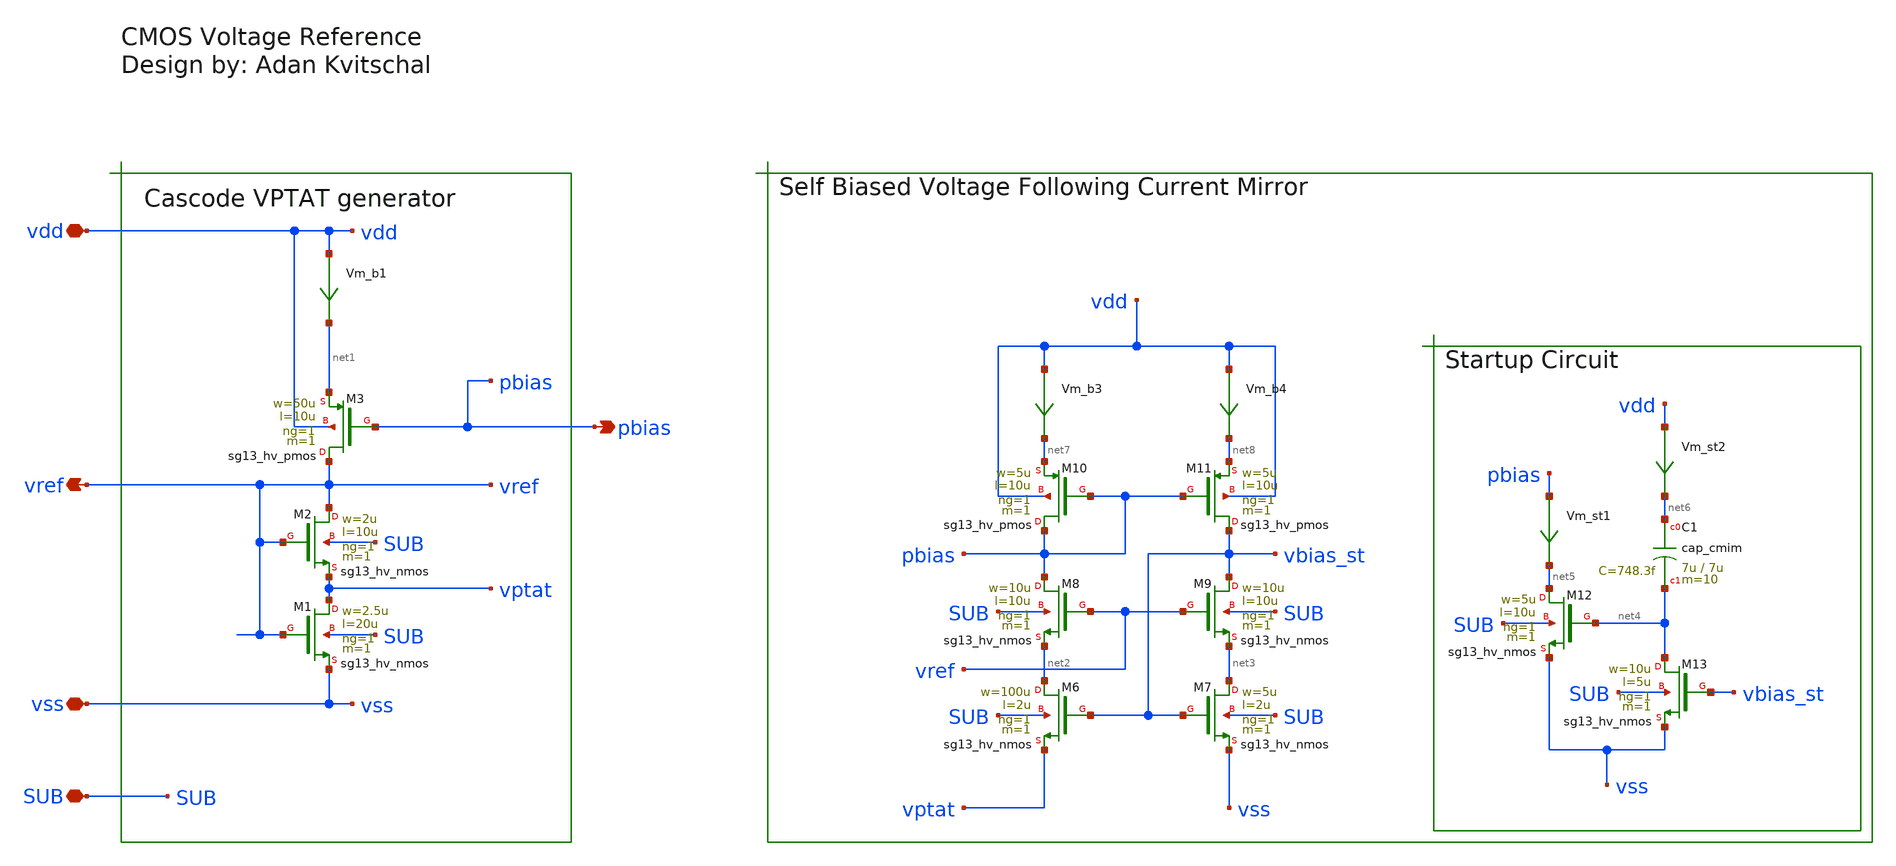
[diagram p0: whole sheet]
** sch_path: release/xschem/sch/cmos_vref.sch
**.subckt cmos_vref vss SUB vdd pbias vref
*.iopin vss
*.iopin SUB
*.iopin vdd
*.opin pbias
*.opin vref
Vm_b1 vdd net1 0
.save i(vm_b1)
XM1 vptat vref vss SUB sg13_hv_nmos w=2.5u l=20u ng=1 m=1 mm_ok=1
XM2 vref vref vptat SUB sg13_hv_nmos w=2u l=10u ng=1 m=1 mm_ok=1
XM3 vref pbias net1 vdd sg13_hv_pmos w=50u l=10u ng=1 m=1 mm_ok=1
Vm_st1 pbias net5 0
.save i(vm_st1)
Vm_st2 vdd net6 0
.save i(vm_st2)
Vm_b3 vdd net7 0
.save i(vm_b3)
Vm_b4 vdd net8 0
.save i(vm_b4)
XM7 net3 vbias_st vss SUB sg13_hv_nmos w=5u l=2u ng=1 m=1 mm_ok=1
XM11 vbias_st pbias net8 vdd sg13_hv_pmos w=5u l=10u ng=1 m=1 mm_ok=1
XM6 net2 vbias_st vptat SUB sg13_hv_nmos w=100u l=2u ng=1 m=1 mm_ok=1
XM9 vbias_st vref net3 SUB sg13_hv_nmos w=10u l=10u ng=1 m=1 mm_ok=1
XM8 pbias vref net2 SUB sg13_hv_nmos w=10u l=10u ng=1 m=1 mm_ok=1
XM10 pbias pbias net7 vdd sg13_hv_pmos w=5u l=10u ng=1 m=1 mm_ok=1
XM13 net4 vbias_st vss SUB sg13_hv_nmos w=10u l=5u ng=1 m=1 mm_ok=1
XM12 net5 net4 vss SUB sg13_hv_nmos w=5u l=10u ng=1 m=1 mm_ok=1
XC1 net6 net4 cap_cmim w=7u l=7u m=10 mm_ok=1
**.ends
.end
